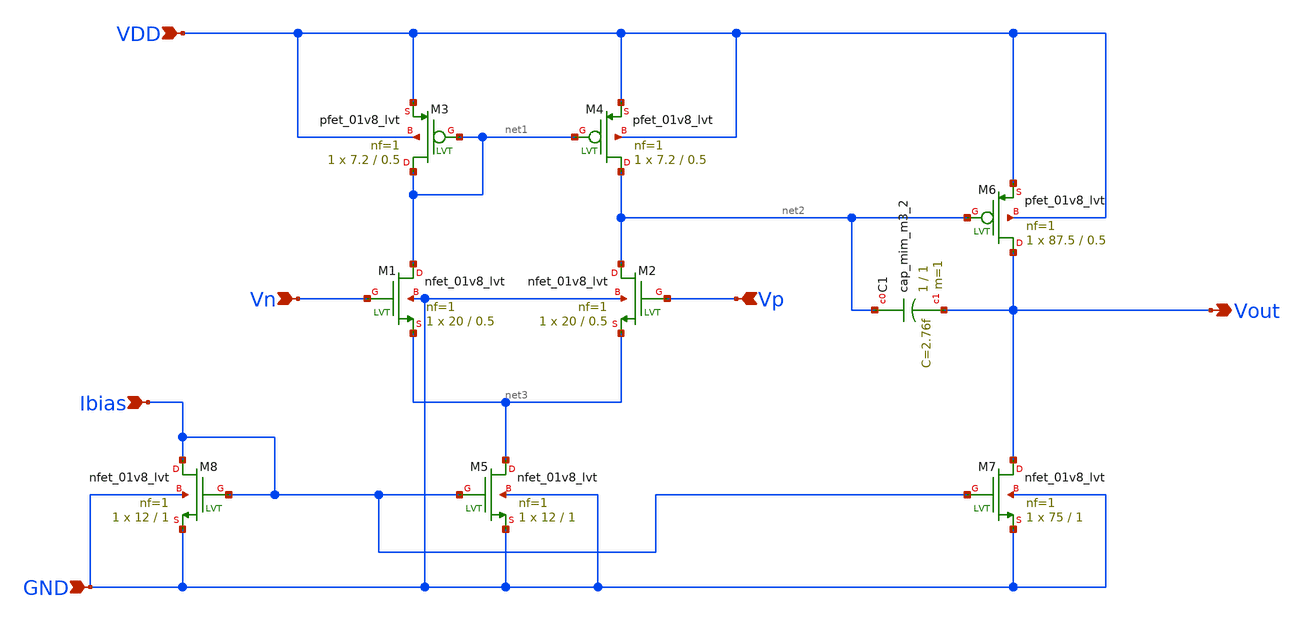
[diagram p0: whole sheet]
** sch_path: Analog_Blocks/OTA/Schematic/Miller_OTA/Transistor1.8v/Miller_OTA_NMOS_1.8v.sch
**.subckt Miller_OTA_NMOS_1.8v Ibias Vn Vp VDD GND Vout
*.ipin Ibias
*.ipin Vn
*.ipin Vp
*.ipin VDD
*.ipin GND
*.opin Vout
XM1 net1 Vn net3 GND sky130_fd_pr__nfet_01v8_lvt L=0.5 W=20 nf=1 ad='int((nf+1)/2) * W/nf * 0.29' as='int((nf+2)/2) * W/nf * 0.29'
+ pd='2*int((nf+1)/2) * (W/nf + 0.29)' ps='2*int((nf+2)/2) * (W/nf + 0.29)' nrd='0.29 / W' nrs='0.29 / W'
+ sa=0 sb=0 sd=0 mult=1 m=1
XM2 net2 Vp net3 GND sky130_fd_pr__nfet_01v8_lvt L=0.5 W=20 nf=1 ad='int((nf+1)/2) * W/nf * 0.29' as='int((nf+2)/2) * W/nf * 0.29'
+ pd='2*int((nf+1)/2) * (W/nf + 0.29)' ps='2*int((nf+2)/2) * (W/nf + 0.29)' nrd='0.29 / W' nrs='0.29 / W'
+ sa=0 sb=0 sd=0 mult=1 m=1
XM5 net3 Ibias GND GND sky130_fd_pr__nfet_01v8_lvt L=1 W=12 nf=1 ad='int((nf+1)/2) * W/nf * 0.29' as='int((nf+2)/2) * W/nf * 0.29'
+ pd='2*int((nf+1)/2) * (W/nf + 0.29)' ps='2*int((nf+2)/2) * (W/nf + 0.29)' nrd='0.29 / W' nrs='0.29 / W'
+ sa=0 sb=0 sd=0 mult=1 m=1
XM8 Ibias Ibias GND GND sky130_fd_pr__nfet_01v8_lvt L=1 W=12 nf=1 ad='int((nf+1)/2) * W/nf * 0.29' as='int((nf+2)/2) * W/nf * 0.29'
+ pd='2*int((nf+1)/2) * (W/nf + 0.29)' ps='2*int((nf+2)/2) * (W/nf + 0.29)' nrd='0.29 / W' nrs='0.29 / W'
+ sa=0 sb=0 sd=0 mult=1 m=1
XM7 Vout Ibias GND GND sky130_fd_pr__nfet_01v8_lvt L=1 W=75 nf=1 ad='int((nf+1)/2) * W/nf * 0.29' as='int((nf+2)/2) * W/nf * 0.29'
+ pd='2*int((nf+1)/2) * (W/nf + 0.29)' ps='2*int((nf+2)/2) * (W/nf + 0.29)' nrd='0.29 / W' nrs='0.29 / W'
+ sa=0 sb=0 sd=0 mult=1 m=1
XM4 net2 net1 VDD VDD sky130_fd_pr__pfet_01v8_lvt L=0.5 W=7.2 nf=1 ad='int((nf+1)/2) * W/nf * 0.29' as='int((nf+2)/2) * W/nf * 0.29'
+ pd='2*int((nf+1)/2) * (W/nf + 0.29)' ps='2*int((nf+2)/2) * (W/nf + 0.29)' nrd='0.29 / W' nrs='0.29 / W'
+ sa=0 sb=0 sd=0 mult=1 m=1
XM3 net1 net1 VDD VDD sky130_fd_pr__pfet_01v8_lvt L=0.5 W=7.2 nf=1 ad='int((nf+1)/2) * W/nf * 0.29' as='int((nf+2)/2) * W/nf * 0.29'
+ pd='2*int((nf+1)/2) * (W/nf + 0.29)' ps='2*int((nf+2)/2) * (W/nf + 0.29)' nrd='0.29 / W' nrs='0.29 / W'
+ sa=0 sb=0 sd=0 mult=1 m=1
XM6 Vout net2 VDD VDD sky130_fd_pr__pfet_01v8_lvt L=0.5 W=87.5 nf=1 ad='int((nf+1)/2) * W/nf * 0.29'
+ as='int((nf+2)/2) * W/nf * 0.29' pd='2*int((nf+1)/2) * (W/nf + 0.29)' ps='2*int((nf+2)/2) * (W/nf + 0.29)'
+ nrd='0.29 / W' nrs='0.29 / W' sa=0 sb=0 sd=0 mult=1 m=1
XC1 net2 Vout sky130_fd_pr__cap_mim_m3_2 W=1 L=1 MF=1 m=1
**.ends
.end
